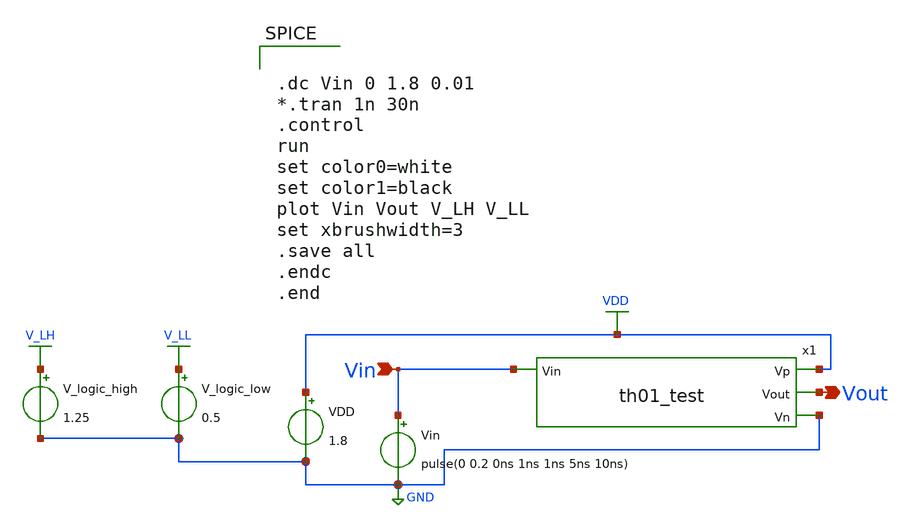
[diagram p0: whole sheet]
** sch_path: xschem/Vth_sch/Pre_layout/th01_test.sch
**.subckt th01_test Vin Vout
*.ipin Vin
*.opin Vout
VDD VDD GND 1.8
Vin Vin GND pulse(0 0.2 0ns 1ns 1ns 5ns 10ns)
V_logic_high V_LH GND 1.25
V_logic_low V_LL GND 0.5
x1 VDD Vout Vin GND th01_test
**** begin user architecture code


.lib /usr/local/share/pdk/sky130A/libs.tech/ngspice/sky130.lib.spice tt

.save all





.dc Vin 0 1.8 0.01
*.tran 1n 30n
.control
run
set color0=white
set color1=black
plot Vin Vout V_LH V_LL
set xbrushwidth=3
.save all
.endc
.end


**** end user architecture code
**.ends

* expanding   symbol:  /home/exotic/Desktop/ASIC_ADC/xschem/Vth_sch/Symbol/th01_test.sym # of pins=4
** sym_path: xschem/Vth_sch/Symbol/th01_test.sym
** sch_path: xschem/Vth_sch/Symbol/th01_test.sch
.subckt th01_test Vp Vout Vin Vn
*.opin Vn
*.opin Vp
*.ipin Vin
*.opin Vout
XM1 Vn Vn net2 net2 sky130_fd_pr__pfet_01v8 L=12 W=0.42 nf=1 ad='int((nf+1)/2) * W/nf * 0.29' as='int((nf+2)/2) * W/nf * 0.29'
+ pd='2*int((nf+1)/2) * (W/nf + 0.29)' ps='2*int((nf+2)/2) * (W/nf + 0.29)' nrd='0.29 / W' nrs='0.29 / W'
+ sa=0 sb=0 sd=0 mult=1 m=1
XM2 Vp Vp net1 net1 sky130_fd_pr__nfet_01v8 L=12 W=0.36 nf=1 ad='int((nf+1)/2) * W/nf * 0.29' as='int((nf+2)/2) * W/nf * 0.29'
+ pd='2*int((nf+1)/2) * (W/nf + 0.29)' ps='2*int((nf+2)/2) * (W/nf + 0.29)' nrd='0.29 / W' nrs='0.29 / W'
+ sa=0 sb=0 sd=0 mult=1 m=1
XM5 net2 Vin Vout Vout sky130_fd_pr__pfet_01v8 L=12 W=0.42 nf=1 ad='int((nf+1)/2) * W/nf * 0.29' as='int((nf+2)/2) * W/nf * 0.29'
+ pd='2*int((nf+1)/2) * (W/nf + 0.29)' ps='2*int((nf+2)/2) * (W/nf + 0.29)' nrd='0.29 / W' nrs='0.29 / W'
+ sa=0 sb=0 sd=0 mult=1 m=1
XM6 net1 Vin Vout Vout sky130_fd_pr__nfet_01v8 L=12 W=0.36 nf=1 ad='int((nf+1)/2) * W/nf * 0.29' as='int((nf+2)/2) * W/nf * 0.29'
+ pd='2*int((nf+1)/2) * (W/nf + 0.29)' ps='2*int((nf+2)/2) * (W/nf + 0.29)' nrd='0.29 / W' nrs='0.29 / W'
+ sa=0 sb=0 sd=0 mult=1 m=1
.ends

.GLOBAL VDD
.GLOBAL GND
.GLOBAL V_LH
.GLOBAL V_LL
.end
